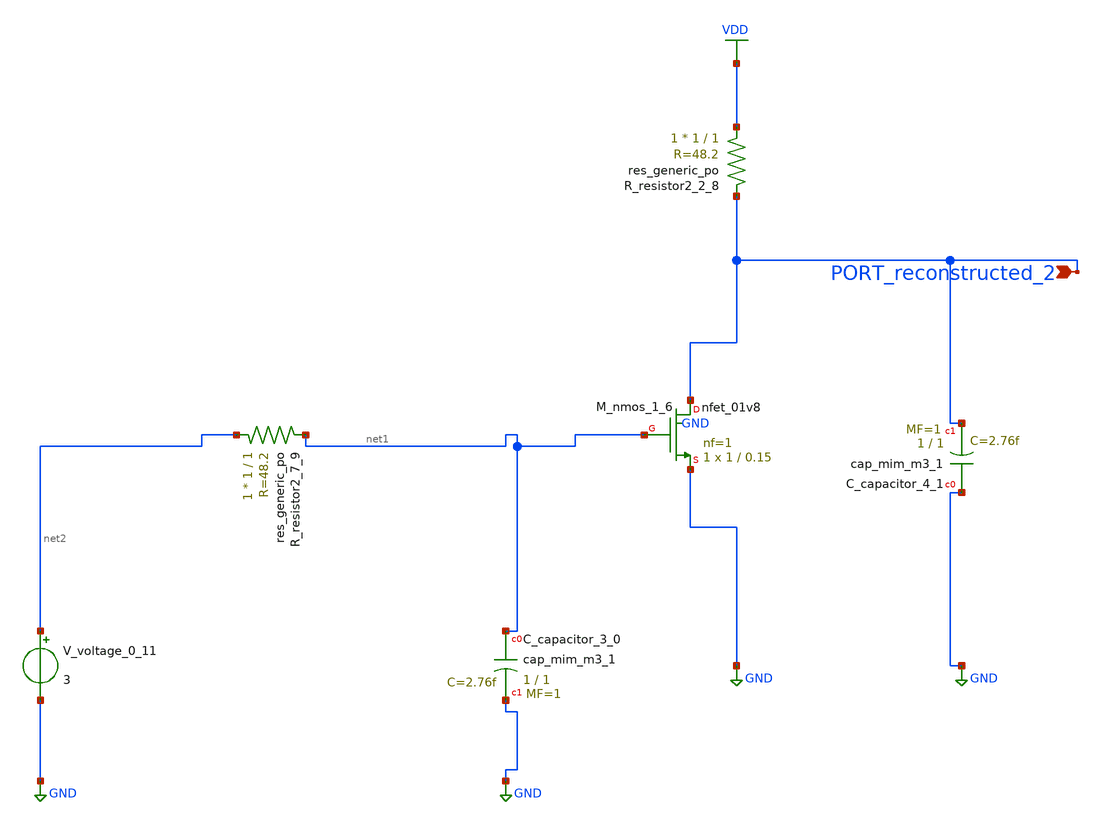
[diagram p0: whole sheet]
** sch_path: schematics/AMSNet/362.sch
**.subckt 362 PORT_reconstructed_2
*.ipin PORT_reconstructed_2
XC_capacitor_3_0 net1 GND sky130_fd_pr__cap_mim_m3_1 W=1 L=1 MF=1 m=1
XC_capacitor_4_1 GND PORT_reconstructed_2 sky130_fd_pr__cap_mim_m3_1 W=1 L=1 MF=1 m=1
XM_nmos_1_6 PORT_reconstructed_2 net1 GND GND sky130_fd_pr__nfet_01v8 L=0.15 W=1 nf=1 ad='int((1 + 1)/2) * 1 / 1 * 0.29'
+ as='int((1 + 2)/2) * 1 / 1 * 0.29' pd='2*int((1 + 1)/2) * (1 / 1 + 0.29)' ps='2*int((1 + 2)/2) * (1 / 1 + 0.29)'
+ nrd='0.29 / 1 ' nrs='0.29 / 1 ' sa=0 sb=0 sd=0 mult=1 m=1
XR_resistor2_2_8 VDD PORT_reconstructed_2 sky130_fd_pr__res_generic_po W=1 L=1 m=1
XR_resistor2_7_9 net2 net1 sky130_fd_pr__res_generic_po W=1 L=1 m=1
V_voltage_0_11 net2 GND 3
**.ends
.GLOBAL GND
.GLOBAL VDD
.end
